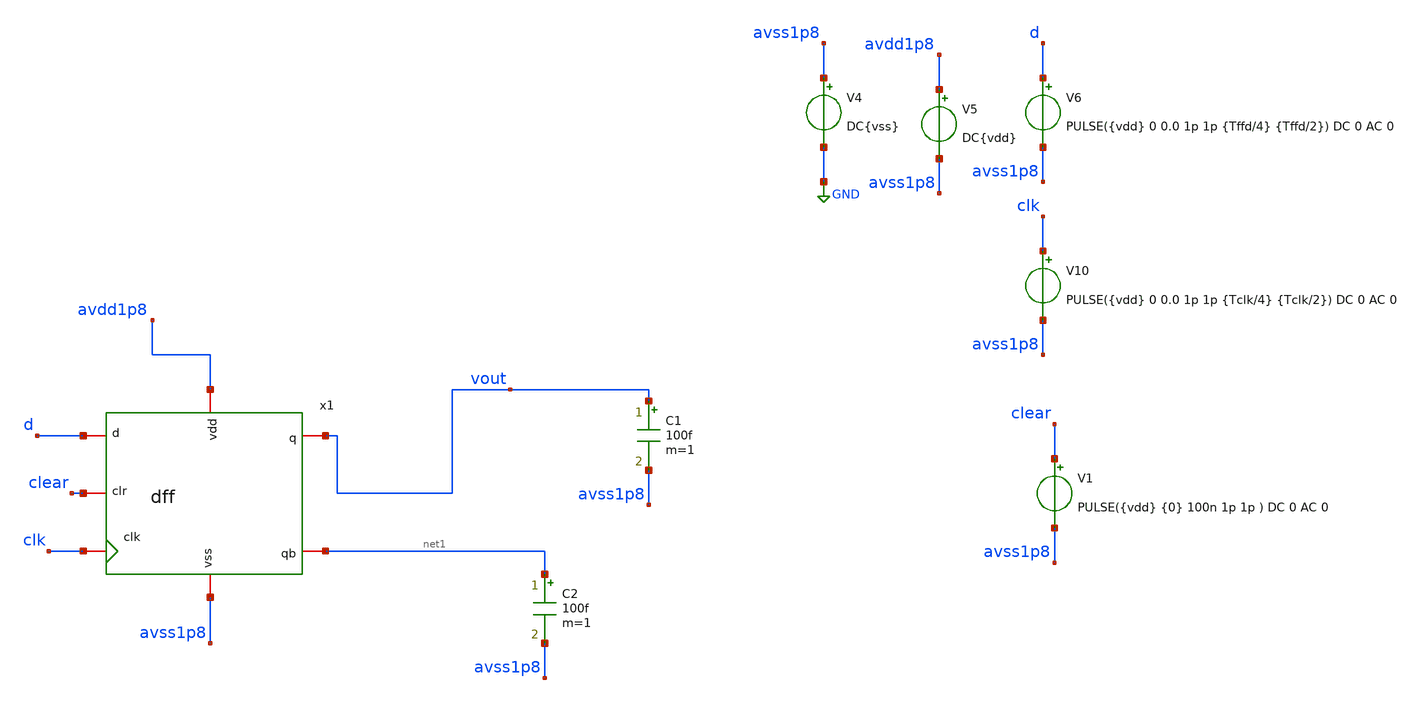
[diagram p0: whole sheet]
** sch_path: verification/testbenches/dff/tb_dff.sch
**.subckt tb_dff
x1 vout net1 d avss1p8 clk clear avdd1p8 dff
C1 vout avss1p8 100f m=1
V4 avss1p8 GND DC{vss}
V6 d avss1p8 PULSE({vdd} 0 0.0 1p 1p {Tffd/4} {Tffd/2}) DC 0 AC 0
V10 clk avss1p8 PULSE({vdd} 0 0.0 1p 1p {Tclk/4} {Tclk/2}) DC 0 AC 0
V5 avdd1p8 avss1p8 DC{vdd}
C2 net1 avss1p8 100f m=1
V1 clear avss1p8 PULSE({vdd} {0} 100n 1p 1p ) DC 0 AC 0
**** begin user architecture code


* Circuit Parameters
.param vdd = 1.2
.param vss = 0.0
.param Tclk = 30n
.param Tffd = 85n
.param Tclear = 200n
.options TEMP = 27.0
* Include Models - IHP SG13G2
.lib cornerMOSlv.lib mos_tt
* OP Parameters & Singals to save
.save all
*Simulations
.control
tran 0.1u 300n
setplot tran1
let prueba1=v(x1.p1)
plot v(d) v(clk)+1.2 v(clear)+2.4 v(vout)+3.6 prueba1+5.8
reset
dc V6 0 1.2 0.01
setplot dc
plot vin vout ylabel vout xlabel vin
set filetype = ascii
write dcsweep.raw
.endc
.end


**** end user architecture code
**.ends
.GLOBAL GND
.end
